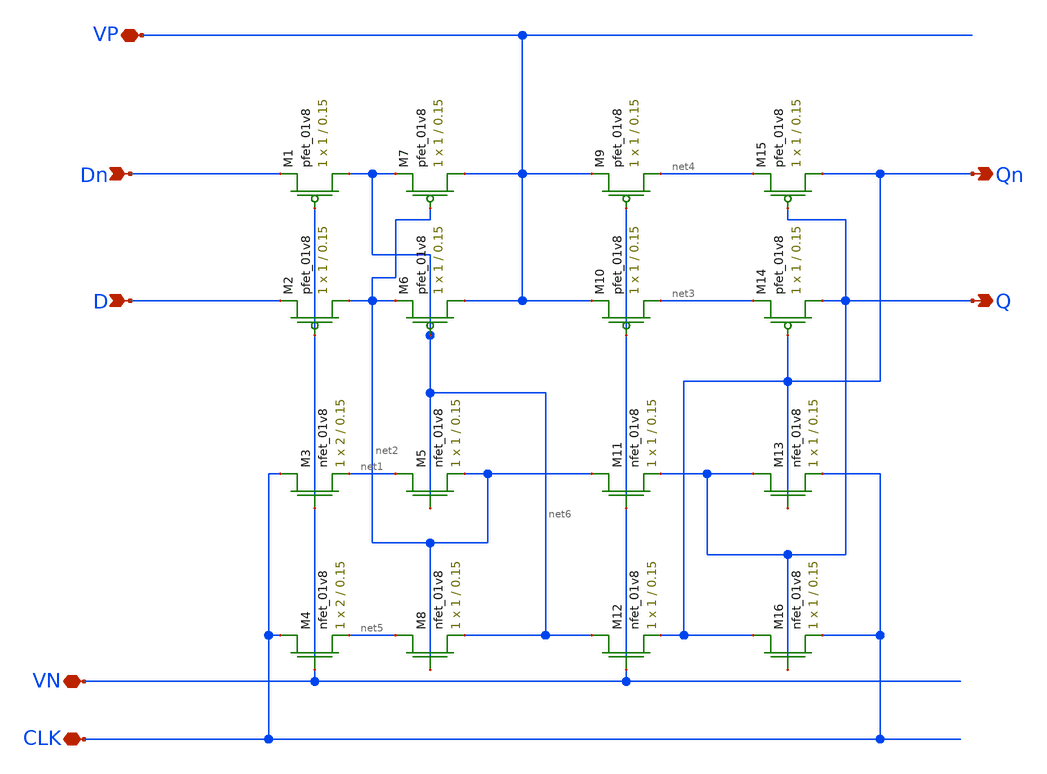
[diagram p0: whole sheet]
** sch_path: MP2/csrl.sch
**.subckt csrl VP VN CLK Dn D Qn Q
*.iopin VP
*.iopin VN
*.iopin CLK
*.ipin Dn
*.ipin D
*.opin Qn
*.opin Q
XM1 net6 VN Dn VDD sky130_fd_pr__pfet_01v8 L=0.15 W=1 nf=1 ad='int((nf+1)/2) * W/nf * 0.29' as='int((nf+2)/2) * W/nf * 0.29'
+ pd='2*int((nf+1)/2) * (W/nf + 0.29)' ps='2*int((nf+2)/2) * (W/nf + 0.29)' nrd='0.29 / W' nrs='0.29 / W'
+ sa=0 sb=0 sd=0 mult=1 m=1
XM2 net2 VN D VDD sky130_fd_pr__pfet_01v8 L=0.15 W=1 nf=1 ad='int((nf+1)/2) * W/nf * 0.29' as='int((nf+2)/2) * W/nf * 0.29'
+ pd='2*int((nf+1)/2) * (W/nf + 0.29)' ps='2*int((nf+2)/2) * (W/nf + 0.29)' nrd='0.29 / W' nrs='0.29 / W'
+ sa=0 sb=0 sd=0 mult=1 m=1
XM3 CLK VN net1 GND sky130_fd_pr__nfet_01v8 L=0.15 W=2 nf=1 ad='int((nf+1)/2) * W/nf * 0.29' as='int((nf+2)/2) * W/nf * 0.29'
+ pd='2*int((nf+1)/2) * (W/nf + 0.29)' ps='2*int((nf+2)/2) * (W/nf + 0.29)' nrd='0.29 / W' nrs='0.29 / W'
+ sa=0 sb=0 sd=0 mult=1 m=1
XM4 CLK VN net5 GND sky130_fd_pr__nfet_01v8 L=0.15 W=2 nf=1 ad='int((nf+1)/2) * W/nf * 0.29' as='int((nf+2)/2) * W/nf * 0.29'
+ pd='2*int((nf+1)/2) * (W/nf + 0.29)' ps='2*int((nf+2)/2) * (W/nf + 0.29)' nrd='0.29 / W' nrs='0.29 / W'
+ sa=0 sb=0 sd=0 mult=1 m=1
XM5 net1 net6 net2 GND sky130_fd_pr__nfet_01v8 L=0.15 W=1 nf=1 ad='int((nf+1)/2) * W/nf * 0.29' as='int((nf+2)/2) * W/nf * 0.29'
+ pd='2*int((nf+1)/2) * (W/nf + 0.29)' ps='2*int((nf+2)/2) * (W/nf + 0.29)' nrd='0.29 / W' nrs='0.29 / W'
+ sa=0 sb=0 sd=0 mult=1 m=1
XM6 VP net6 net2 VDD sky130_fd_pr__pfet_01v8 L=0.15 W=1 nf=1 ad='int((nf+1)/2) * W/nf * 0.29' as='int((nf+2)/2) * W/nf * 0.29'
+ pd='2*int((nf+1)/2) * (W/nf + 0.29)' ps='2*int((nf+2)/2) * (W/nf + 0.29)' nrd='0.29 / W' nrs='0.29 / W'
+ sa=0 sb=0 sd=0 mult=1 m=1
XM7 VP net2 net6 VDD sky130_fd_pr__pfet_01v8 L=0.15 W=1 nf=1 ad='int((nf+1)/2) * W/nf * 0.29' as='int((nf+2)/2) * W/nf * 0.29'
+ pd='2*int((nf+1)/2) * (W/nf + 0.29)' ps='2*int((nf+2)/2) * (W/nf + 0.29)' nrd='0.29 / W' nrs='0.29 / W'
+ sa=0 sb=0 sd=0 mult=1 m=1
XM8 net5 net2 net6 GND sky130_fd_pr__nfet_01v8 L=0.15 W=1 nf=1 ad='int((nf+1)/2) * W/nf * 0.29' as='int((nf+2)/2) * W/nf * 0.29'
+ pd='2*int((nf+1)/2) * (W/nf + 0.29)' ps='2*int((nf+2)/2) * (W/nf + 0.29)' nrd='0.29 / W' nrs='0.29 / W'
+ sa=0 sb=0 sd=0 mult=1 m=1
XM9 net4 VN VP VDD sky130_fd_pr__pfet_01v8 L=0.15 W=1 nf=1 ad='int((nf+1)/2) * W/nf * 0.29' as='int((nf+2)/2) * W/nf * 0.29'
+ pd='2*int((nf+1)/2) * (W/nf + 0.29)' ps='2*int((nf+2)/2) * (W/nf + 0.29)' nrd='0.29 / W' nrs='0.29 / W'
+ sa=0 sb=0 sd=0 mult=1 m=1
XM10 net3 VN VP VDD sky130_fd_pr__pfet_01v8 L=0.15 W=1 nf=1 ad='int((nf+1)/2) * W/nf * 0.29' as='int((nf+2)/2) * W/nf * 0.29'
+ pd='2*int((nf+1)/2) * (W/nf + 0.29)' ps='2*int((nf+2)/2) * (W/nf + 0.29)' nrd='0.29 / W' nrs='0.29 / W'
+ sa=0 sb=0 sd=0 mult=1 m=1
XM11 net2 VN Q GND sky130_fd_pr__nfet_01v8 L=0.15 W=1 nf=1 ad='int((nf+1)/2) * W/nf * 0.29' as='int((nf+2)/2) * W/nf * 0.29'
+ pd='2*int((nf+1)/2) * (W/nf + 0.29)' ps='2*int((nf+2)/2) * (W/nf + 0.29)' nrd='0.29 / W' nrs='0.29 / W'
+ sa=0 sb=0 sd=0 mult=1 m=1
XM12 net6 VN Qn GND sky130_fd_pr__nfet_01v8 L=0.15 W=1 nf=1 ad='int((nf+1)/2) * W/nf * 0.29' as='int((nf+2)/2) * W/nf * 0.29'
+ pd='2*int((nf+1)/2) * (W/nf + 0.29)' ps='2*int((nf+2)/2) * (W/nf + 0.29)' nrd='0.29 / W' nrs='0.29 / W'
+ sa=0 sb=0 sd=0 mult=1 m=1
XM13 Q Qn CLK GND sky130_fd_pr__nfet_01v8 L=0.15 W=1 nf=1 ad='int((nf+1)/2) * W/nf * 0.29' as='int((nf+2)/2) * W/nf * 0.29'
+ pd='2*int((nf+1)/2) * (W/nf + 0.29)' ps='2*int((nf+2)/2) * (W/nf + 0.29)' nrd='0.29 / W' nrs='0.29 / W'
+ sa=0 sb=0 sd=0 mult=1 m=1
XM14 Q Qn net3 VDD sky130_fd_pr__pfet_01v8 L=0.15 W=1 nf=1 ad='int((nf+1)/2) * W/nf * 0.29' as='int((nf+2)/2) * W/nf * 0.29'
+ pd='2*int((nf+1)/2) * (W/nf + 0.29)' ps='2*int((nf+2)/2) * (W/nf + 0.29)' nrd='0.29 / W' nrs='0.29 / W'
+ sa=0 sb=0 sd=0 mult=1 m=1
XM15 Qn Q net4 VDD sky130_fd_pr__pfet_01v8 L=0.15 W=1 nf=1 ad='int((nf+1)/2) * W/nf * 0.29' as='int((nf+2)/2) * W/nf * 0.29'
+ pd='2*int((nf+1)/2) * (W/nf + 0.29)' ps='2*int((nf+2)/2) * (W/nf + 0.29)' nrd='0.29 / W' nrs='0.29 / W'
+ sa=0 sb=0 sd=0 mult=1 m=1
XM16 Qn Q CLK GND sky130_fd_pr__nfet_01v8 L=0.15 W=1 nf=1 ad='int((nf+1)/2) * W/nf * 0.29' as='int((nf+2)/2) * W/nf * 0.29'
+ pd='2*int((nf+1)/2) * (W/nf + 0.29)' ps='2*int((nf+2)/2) * (W/nf + 0.29)' nrd='0.29 / W' nrs='0.29 / W'
+ sa=0 sb=0 sd=0 mult=1 m=1
**.ends
.end
